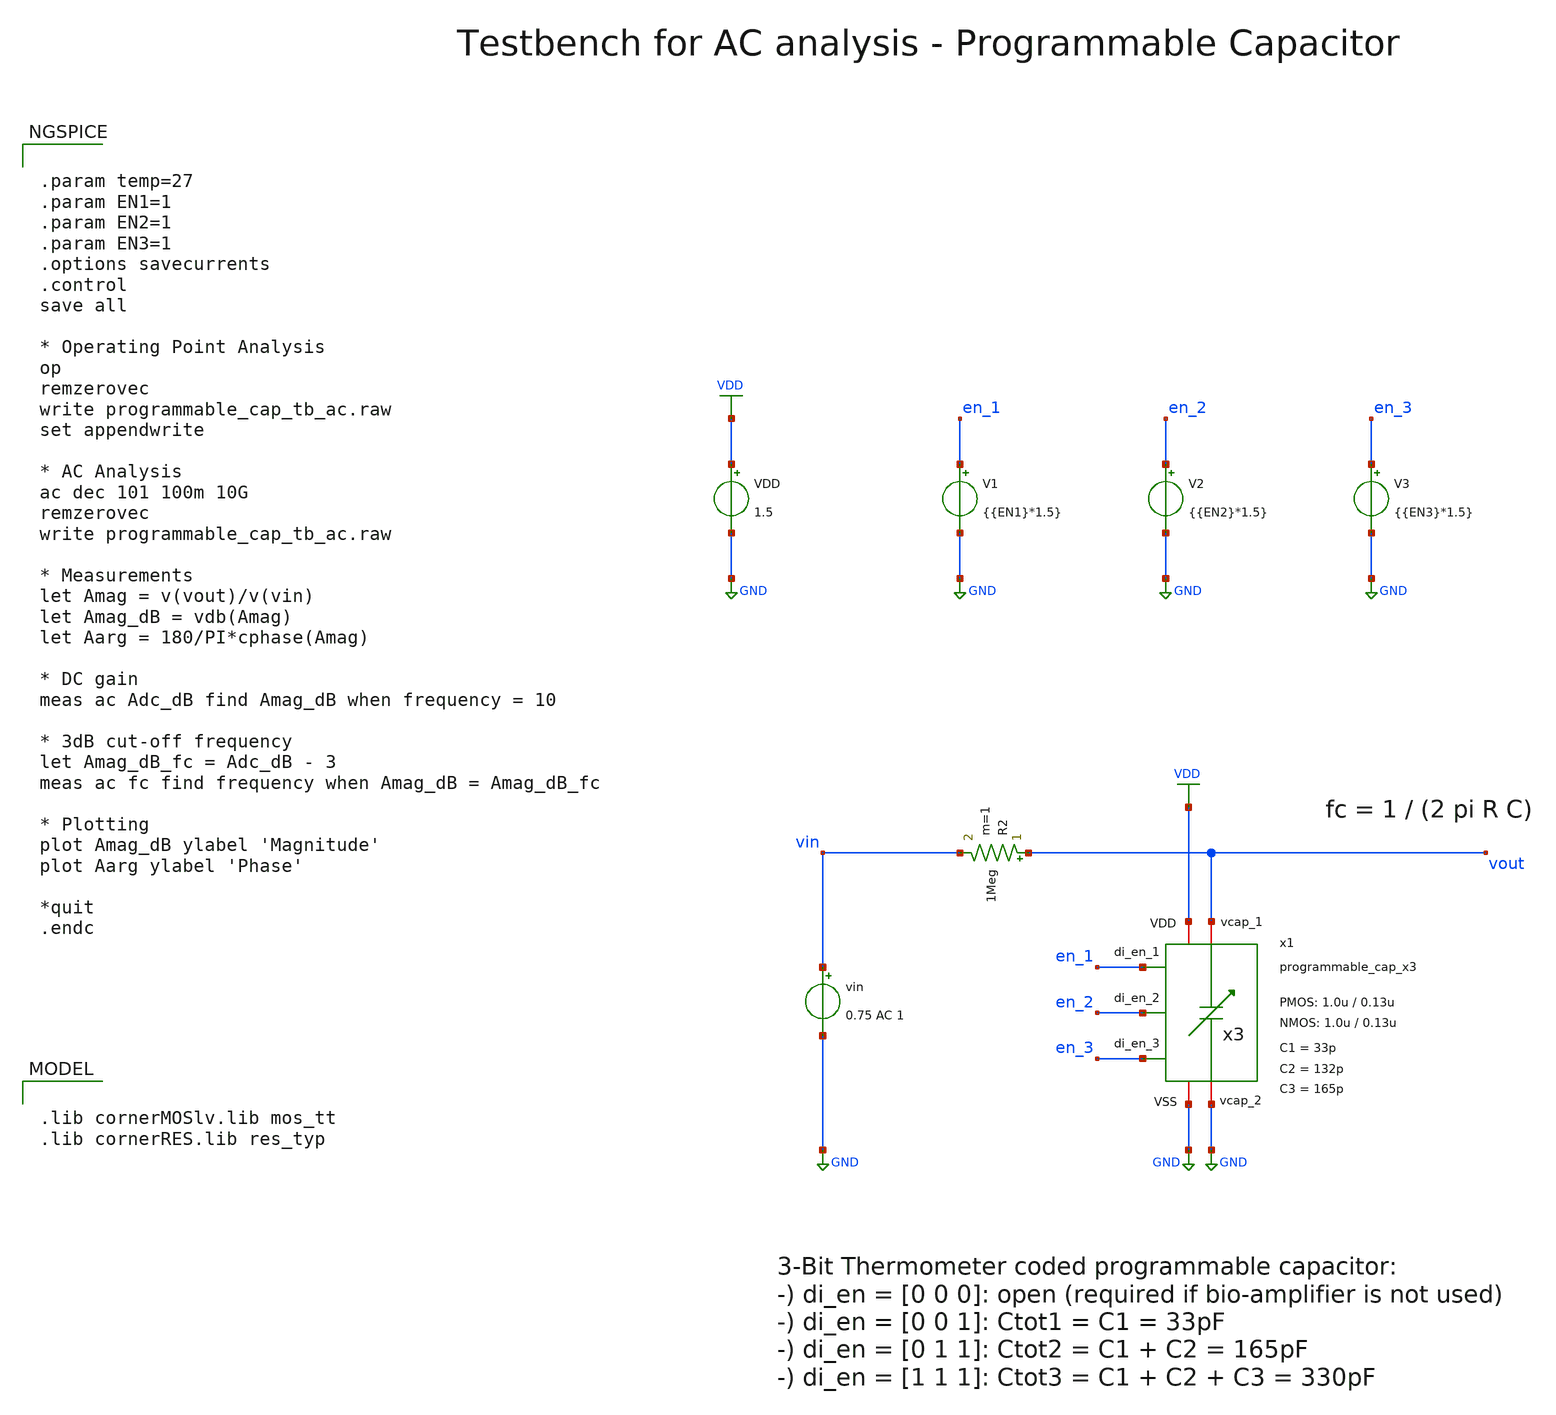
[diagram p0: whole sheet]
** sch_path: SG13G2_ATBS-ADC-main/xschem/programmable_cap/testbenches/programmable_cap_tb_ac.sch
**.subckt programmable_cap_tb_ac
R2 vout vin 1Meg m=1
VDD VDD GND 1.5
V1 en_1 GND {{EN1}*1.5}
V2 en_2 GND {{EN2}*1.5}
V3 en_3 GND {{EN3}*1.5}
x1 VDD en_1 GND en_2 vout GND en_3 programmable_cap_x3 W_P_PC=1.0u L_P_PC=0.13u W_N_PC=1.0u
+ L_N_PC=0.13u C1=33p C2=132p C3=165p
vin vin GND 0.75 AC 1
**** begin user architecture code


.param temp=27
.param EN1=1
.param EN2=1
.param EN3=1
.options savecurrents
.control
save all

* Operating Point Analysis
op
remzerovec
write programmable_cap_tb_ac.raw
set appendwrite

* AC Analysis
ac dec 101 100m 10G
remzerovec
write programmable_cap_tb_ac.raw

* Measurements
let Amag = v(vout)/v(vin)
let Amag_dB = vdb(Amag)
let Aarg = 180/PI*cphase(Amag)

* DC gain
meas ac Adc_dB find Amag_dB when frequency = 10

* 3dB cut-off frequency
let Amag_dB_fc = Adc_dB - 3
meas ac fc find frequency when Amag_dB = Amag_dB_fc

* Plotting
plot Amag_dB ylabel 'Magnitude'
plot Aarg ylabel 'Phase'

*quit
.endc


.lib cornerMOSlv.lib mos_tt
.lib cornerRES.lib res_typ

**** end user architecture code
**.ends

* expanding   symbol:  programmable_cap/programmable_cap_x3.sym # of pins=7
** sym_path: SG13G2_ATBS-ADC-main/xschem/programmable_cap/programmable_cap_x3.sym
** sch_path: SG13G2_ATBS-ADC-main/xschem/programmable_cap/programmable_cap_x3.sch
.subckt programmable_cap_x3 VDD di_en_1 VSS di_en_2 vcap_1 vcap_2 di_en_3  W_P_PC=1.0u L_P_PC=0.13u
+ W_N_PC=1.0u L_N_PC=0.13u C1=33p C2=132p C3=165p
*.iopin vcap_1
*.iopin vcap_2
*.ipin di_en_1
*.ipin di_en_2
*.ipin di_en_3
*.iopin VDD
*.iopin VSS
x6 VDD di_en_3 VSS net2 vcap_1 di_en_3_n transmission_gate_lv_wo_dummy W_P=W_P_PC L_P=L_P_PC
+ W_N=W_N_PC L_N=L_N_PC
x5 VDD di_en_2 VSS net3 vcap_1 di_en_2_n transmission_gate_lv_wo_dummy W_P=W_P_PC L_P=L_P_PC
+ W_N=W_N_PC L_N=L_N_PC
x4 VDD di_en_1 VSS net1 vcap_1 di_en_1_n transmission_gate_lv_wo_dummy W_P=W_P_PC L_P=L_P_PC
+ W_N=W_N_PC L_N=L_N_PC
C3 net2 vcap_2 C3 m=1
C2 net3 vcap_2 C2 m=1
C1 net1 vcap_2 C1 m=1
x1 VDD di_en_1 di_en_1_n VSS inverter_lv W_P=W_P_PC L_P=L_P_PC W_N=W_N_PC L_N=L_N_PC
x2 VDD di_en_2 di_en_2_n VSS inverter_lv W_P=W_P_PC L_P=L_P_PC W_N=W_N_PC L_N=L_N_PC
x3 VDD di_en_3 di_en_3_n VSS inverter_lv W_P=W_P_PC L_P=L_P_PC W_N=W_N_PC L_N=L_N_PC
.ends


* expanding   symbol:  transmission_gate/transmission_gate_lv_wo_dummy.sym # of pins=6
** sym_path: SG13G2_ATBS-ADC-main/xschem/transmission_gate/transmission_gate_lv_wo_dummy.sym
** sch_path: SG13G2_ATBS-ADC-main/xschem/transmission_gate/transmission_gate_lv_wo_dummy.sch
.subckt transmission_gate_lv_wo_dummy VDD di_tg_ctrl VSS v_b v_a di_tg_ctrl_n  W_P=1.0u L_P=0.13u
+ W_N=1.0u L_N=0.13u
*.iopin v_a
*.iopin v_b
*.iopin VDD
*.iopin VSS
*.ipin di_tg_ctrl
*.ipin di_tg_ctrl_n
XM1 v_a di_tg_ctrl v_b VSS sg13_lv_nmos w=W_N l=L_N ng=1 m=1 mm_ok=1
XM2 v_a di_tg_ctrl_n v_b VDD sg13_lv_pmos w=W_P l=L_P ng=1 m=1 mm_ok=1
.ends


* expanding   symbol:  inverter/inverter_lv.sym # of pins=4
** sym_path: SG13G2_ATBS-ADC-main/xschem/inverter/inverter_lv.sym
** sch_path: SG13G2_ATBS-ADC-main/xschem/inverter/inverter_lv.sch
.subckt inverter_lv VDD vin vout VSS  W_P=3.0u L_P=0.13u W_N=1.0u L_N=0.13u
*.ipin vin
*.iopin VDD
*.iopin VSS
*.opin vout
XM1 vout vin VDD VDD sg13_lv_pmos w=W_P l=L_P ng=1 m=1 mm_ok=1
XM2 vout vin VSS VSS sg13_lv_nmos w=W_N l=L_N ng=1 m=1 mm_ok=1
.ends

.GLOBAL GND
.GLOBAL VDD
.end
